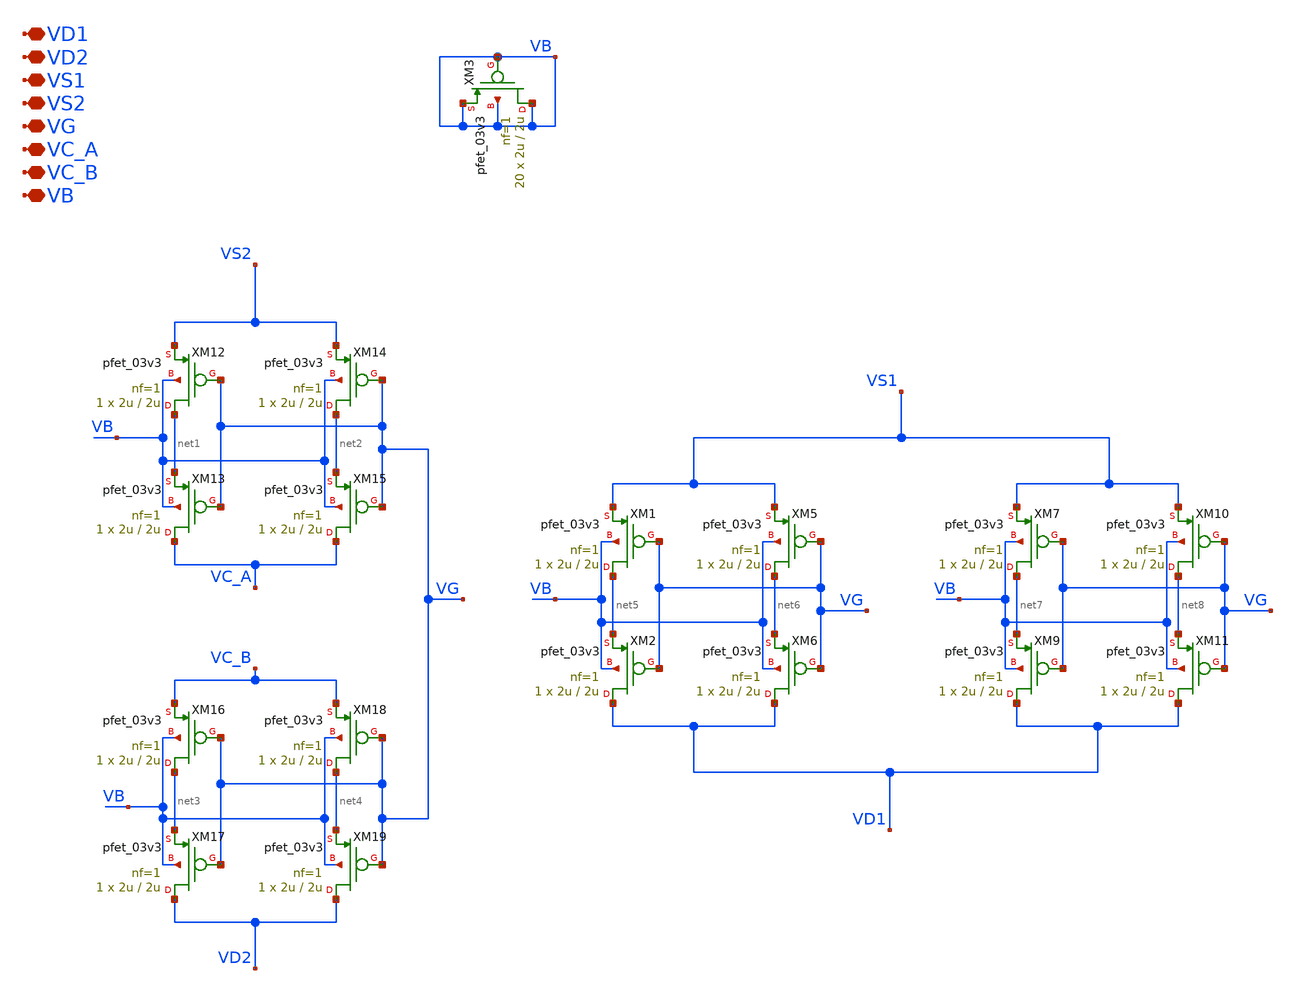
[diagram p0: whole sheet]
** sch_path: TIA/xschem/PseudoResistor/PR_pfets.sch
**.subckt PR_pfets VD1 VD2 VS1 VS2 VG VC_A VC_B VB
*.iopin VD1
*.iopin VD2
*.iopin VS1
*.iopin VS2
*.iopin VG
*.iopin VC_A
*.iopin VC_B
*.iopin VB
XM1 net5 VG VS1 VB pfet_03v3 L=2u W=2u nf=1 ad='int((nf+1)/2) * W/nf * 0.18u' as='int((nf+2)/2) * W/nf * 0.18u'
+ pd='2*int((nf+1)/2) * (W/nf + 0.18u)' ps='2*int((nf+2)/2) * (W/nf + 0.18u)' nrd='0.18u / W' nrs='0.18u / W'
+ sa=0 sb=0 sd=0 m=1
XM2 VD1 VG net5 VB pfet_03v3 L=2u W=2u nf=1 ad='int((nf+1)/2) * W/nf * 0.18u' as='int((nf+2)/2) * W/nf * 0.18u'
+ pd='2*int((nf+1)/2) * (W/nf + 0.18u)' ps='2*int((nf+2)/2) * (W/nf + 0.18u)' nrd='0.18u / W' nrs='0.18u / W'
+ sa=0 sb=0 sd=0 m=1
XM5 net6 VG VS1 VB pfet_03v3 L=2u W=2u nf=1 ad='int((nf+1)/2) * W/nf * 0.18u' as='int((nf+2)/2) * W/nf * 0.18u'
+ pd='2*int((nf+1)/2) * (W/nf + 0.18u)' ps='2*int((nf+2)/2) * (W/nf + 0.18u)' nrd='0.18u / W' nrs='0.18u / W'
+ sa=0 sb=0 sd=0 m=1
XM6 VD1 VG net6 VB pfet_03v3 L=2u W=2u nf=1 ad='int((nf+1)/2) * W/nf * 0.18u' as='int((nf+2)/2) * W/nf * 0.18u'
+ pd='2*int((nf+1)/2) * (W/nf + 0.18u)' ps='2*int((nf+2)/2) * (W/nf + 0.18u)' nrd='0.18u / W' nrs='0.18u / W'
+ sa=0 sb=0 sd=0 m=1
XM7 net7 VG VS1 VB pfet_03v3 L=2u W=2u nf=1 ad='int((nf+1)/2) * W/nf * 0.18u' as='int((nf+2)/2) * W/nf * 0.18u'
+ pd='2*int((nf+1)/2) * (W/nf + 0.18u)' ps='2*int((nf+2)/2) * (W/nf + 0.18u)' nrd='0.18u / W' nrs='0.18u / W'
+ sa=0 sb=0 sd=0 m=1
XM9 VD1 VG net7 VB pfet_03v3 L=2u W=2u nf=1 ad='int((nf+1)/2) * W/nf * 0.18u' as='int((nf+2)/2) * W/nf * 0.18u'
+ pd='2*int((nf+1)/2) * (W/nf + 0.18u)' ps='2*int((nf+2)/2) * (W/nf + 0.18u)' nrd='0.18u / W' nrs='0.18u / W'
+ sa=0 sb=0 sd=0 m=1
XM10 net8 VG VS1 VB pfet_03v3 L=2u W=2u nf=1 ad='int((nf+1)/2) * W/nf * 0.18u' as='int((nf+2)/2) * W/nf * 0.18u'
+ pd='2*int((nf+1)/2) * (W/nf + 0.18u)' ps='2*int((nf+2)/2) * (W/nf + 0.18u)' nrd='0.18u / W' nrs='0.18u / W'
+ sa=0 sb=0 sd=0 m=1
XM11 VD1 VG net8 VB pfet_03v3 L=2u W=2u nf=1 ad='int((nf+1)/2) * W/nf * 0.18u' as='int((nf+2)/2) * W/nf * 0.18u'
+ pd='2*int((nf+1)/2) * (W/nf + 0.18u)' ps='2*int((nf+2)/2) * (W/nf + 0.18u)' nrd='0.18u / W' nrs='0.18u / W'
+ sa=0 sb=0 sd=0 m=1
XM12 net1 VG VS2 VB pfet_03v3 L=2u W=2u nf=1 ad='int((nf+1)/2) * W/nf * 0.18u' as='int((nf+2)/2) * W/nf * 0.18u'
+ pd='2*int((nf+1)/2) * (W/nf + 0.18u)' ps='2*int((nf+2)/2) * (W/nf + 0.18u)' nrd='0.18u / W' nrs='0.18u / W'
+ sa=0 sb=0 sd=0 m=1
XM13 VC_A VG net1 VB pfet_03v3 L=2u W=2u nf=1 ad='int((nf+1)/2) * W/nf * 0.18u' as='int((nf+2)/2) * W/nf * 0.18u'
+ pd='2*int((nf+1)/2) * (W/nf + 0.18u)' ps='2*int((nf+2)/2) * (W/nf + 0.18u)' nrd='0.18u / W' nrs='0.18u / W'
+ sa=0 sb=0 sd=0 m=1
XM14 net2 VG VS2 VB pfet_03v3 L=2u W=2u nf=1 ad='int((nf+1)/2) * W/nf * 0.18u' as='int((nf+2)/2) * W/nf * 0.18u'
+ pd='2*int((nf+1)/2) * (W/nf + 0.18u)' ps='2*int((nf+2)/2) * (W/nf + 0.18u)' nrd='0.18u / W' nrs='0.18u / W'
+ sa=0 sb=0 sd=0 m=1
XM15 VC_A VG net2 VB pfet_03v3 L=2u W=2u nf=1 ad='int((nf+1)/2) * W/nf * 0.18u' as='int((nf+2)/2) * W/nf * 0.18u'
+ pd='2*int((nf+1)/2) * (W/nf + 0.18u)' ps='2*int((nf+2)/2) * (W/nf + 0.18u)' nrd='0.18u / W' nrs='0.18u / W'
+ sa=0 sb=0 sd=0 m=1
XM16 net3 VG VC_B VB pfet_03v3 L=2u W=2u nf=1 ad='int((nf+1)/2) * W/nf * 0.18u' as='int((nf+2)/2) * W/nf * 0.18u'
+ pd='2*int((nf+1)/2) * (W/nf + 0.18u)' ps='2*int((nf+2)/2) * (W/nf + 0.18u)' nrd='0.18u / W' nrs='0.18u / W'
+ sa=0 sb=0 sd=0 m=1
XM17 VD2 VG net3 VB pfet_03v3 L=2u W=2u nf=1 ad='int((nf+1)/2) * W/nf * 0.18u' as='int((nf+2)/2) * W/nf * 0.18u'
+ pd='2*int((nf+1)/2) * (W/nf + 0.18u)' ps='2*int((nf+2)/2) * (W/nf + 0.18u)' nrd='0.18u / W' nrs='0.18u / W'
+ sa=0 sb=0 sd=0 m=1
XM18 net4 VG VC_B VB pfet_03v3 L=2u W=2u nf=1 ad='int((nf+1)/2) * W/nf * 0.18u' as='int((nf+2)/2) * W/nf * 0.18u'
+ pd='2*int((nf+1)/2) * (W/nf + 0.18u)' ps='2*int((nf+2)/2) * (W/nf + 0.18u)' nrd='0.18u / W' nrs='0.18u / W'
+ sa=0 sb=0 sd=0 m=1
XM19 VD2 VG net4 VB pfet_03v3 L=2u W=2u nf=1 ad='int((nf+1)/2) * W/nf * 0.18u' as='int((nf+2)/2) * W/nf * 0.18u'
+ pd='2*int((nf+1)/2) * (W/nf + 0.18u)' ps='2*int((nf+2)/2) * (W/nf + 0.18u)' nrd='0.18u / W' nrs='0.18u / W'
+ sa=0 sb=0 sd=0 m=1
XM3 VB VB VB VB pfet_03v3 L=2u W=2u nf=1 ad='int((nf+1)/2) * W/nf * 0.18u' as='int((nf+2)/2) * W/nf * 0.18u'
+ pd='2*int((nf+1)/2) * (W/nf + 0.18u)' ps='2*int((nf+2)/2) * (W/nf + 0.18u)' nrd='0.18u / W' nrs='0.18u / W'
+ sa=0 sb=0 sd=0 m=20
**.ends
.end
